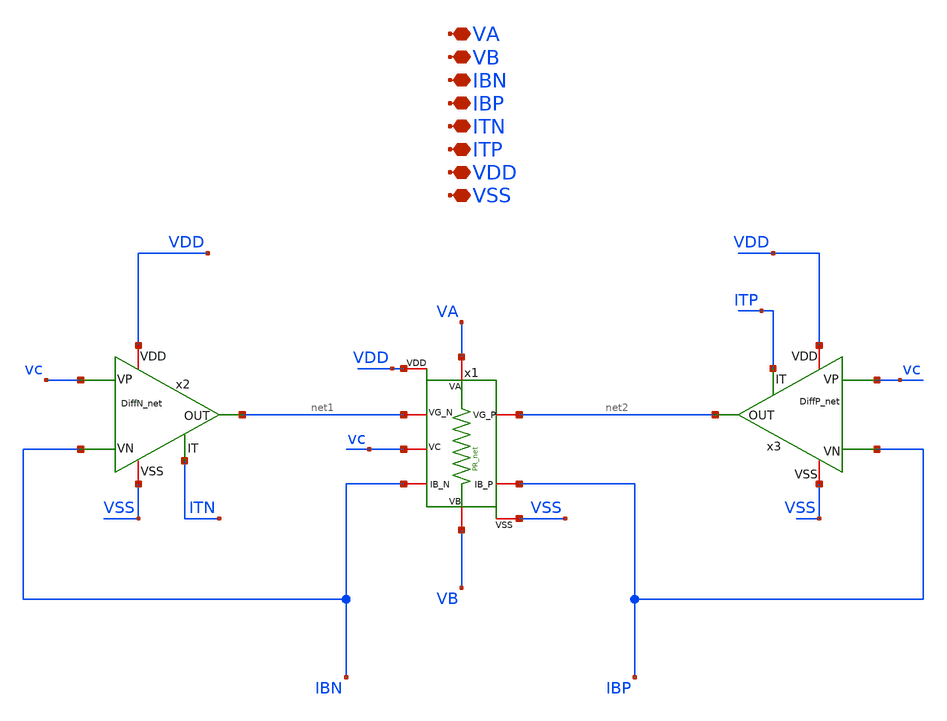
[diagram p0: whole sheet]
** sch_path: TIA_Filter/PseudoResistor/PRbiased_net.sch
**.subckt PRbiased_net VA VB IBN IBP ITN ITP VDD VSS
*.iopin VA
*.iopin VB
*.iopin IBN
*.iopin IBP
*.iopin ITN
*.iopin ITP
*.iopin VDD
*.iopin VSS
x1 VA VB net1 net2 IBN IBP vc VDD VSS PR_net
x2 IBN vc net1 ITN VDD VSS DiffN_net
x3 IBP vc net2 ITP VDD VSS DiffP_net
**.ends
.end
